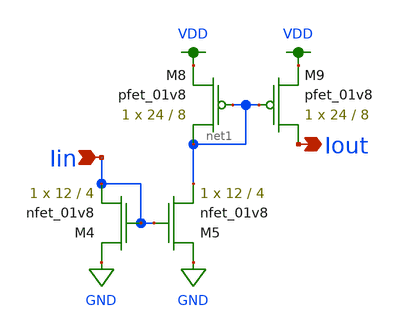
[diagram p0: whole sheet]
** sch_path: simple_mirror_source.sch
**.subckt simple_mirror_source Iin Iout
*.ipin Iin
*.opin Iout
XM4 GND Iin Iin GND sky130_fd_pr__nfet_01v8 L=4 W=12 nf=1 ad='int((nf+1)/2) * W/nf * 0.29' as='int((nf+2)/2) * W/nf * 0.29'
+ pd='2*int((nf+1)/2) * (W/nf + 0.29)' ps='2*int((nf+2)/2) * (W/nf + 0.29)' nrd='0.29 / W' nrs='0.29 / W'
+ sa=0 sb=0 sd=0 mult=1 m=1
XM5 GND Iin net1 GND sky130_fd_pr__nfet_01v8 L=4 W=12 nf=1 ad='int((nf+1)/2) * W/nf * 0.29' as='int((nf+2)/2) * W/nf * 0.29'
+ pd='2*int((nf+1)/2) * (W/nf + 0.29)' ps='2*int((nf+2)/2) * (W/nf + 0.29)' nrd='0.29 / W' nrs='0.29 / W'
+ sa=0 sb=0 sd=0 mult=1 m=1
XM8 net1 net1 VDD VDD sky130_fd_pr__pfet_01v8 L=8 W=24 nf=1 ad='int((nf+1)/2) * W/nf * 0.29' as='int((nf+2)/2) * W/nf * 0.29'
+ pd='2*int((nf+1)/2) * (W/nf + 0.29)' ps='2*int((nf+2)/2) * (W/nf + 0.29)' nrd='0.29 / W' nrs='0.29 / W'
+ sa=0 sb=0 sd=0 mult=1 m=1
XM9 Iout net1 VDD VDD sky130_fd_pr__pfet_01v8 L=8 W=24 nf=1 ad='int((nf+1)/2) * W/nf * 0.29' as='int((nf+2)/2) * W/nf * 0.29'
+ pd='2*int((nf+1)/2) * (W/nf + 0.29)' ps='2*int((nf+2)/2) * (W/nf + 0.29)' nrd='0.29 / W' nrs='0.29 / W'
+ sa=0 sb=0 sd=0 mult=1 m=1
**.ends
.GLOBAL GND
.GLOBAL VDD
.end
